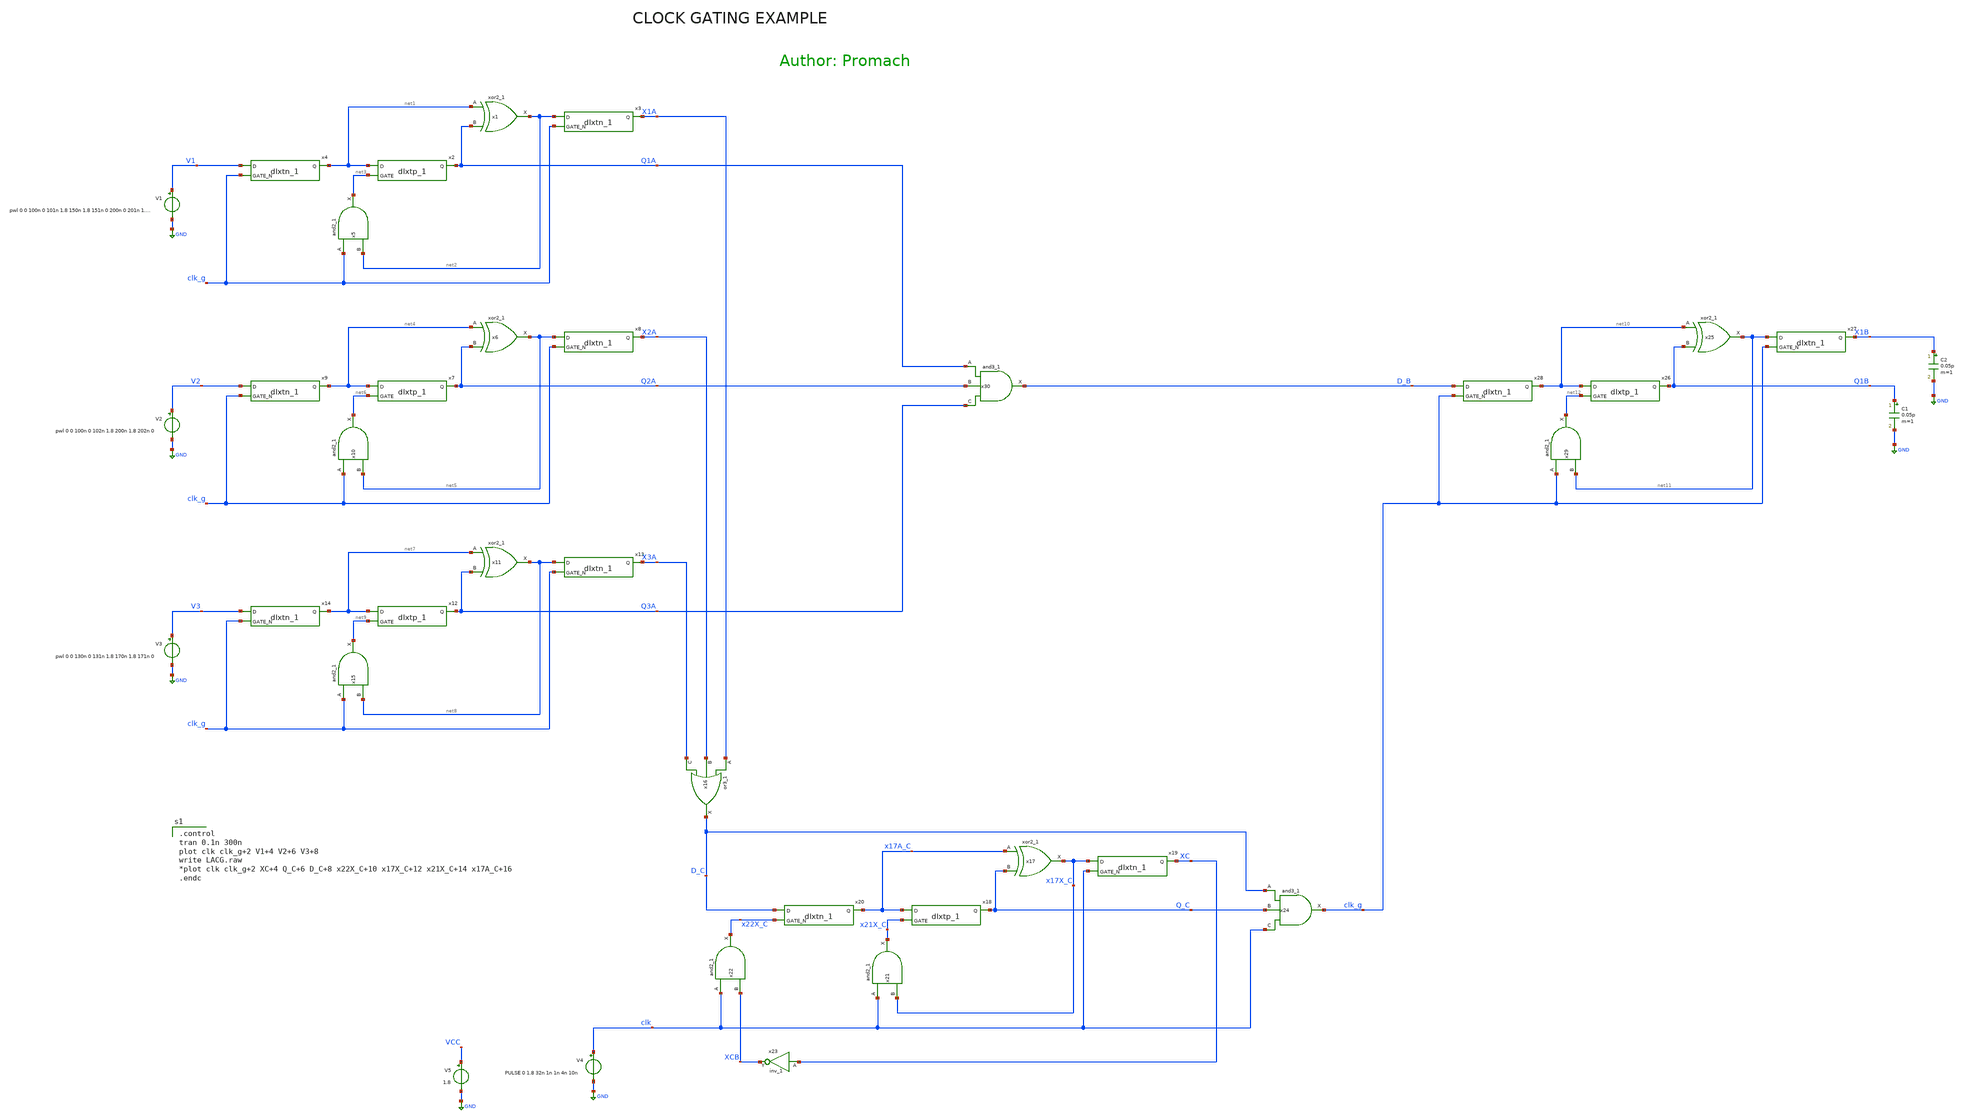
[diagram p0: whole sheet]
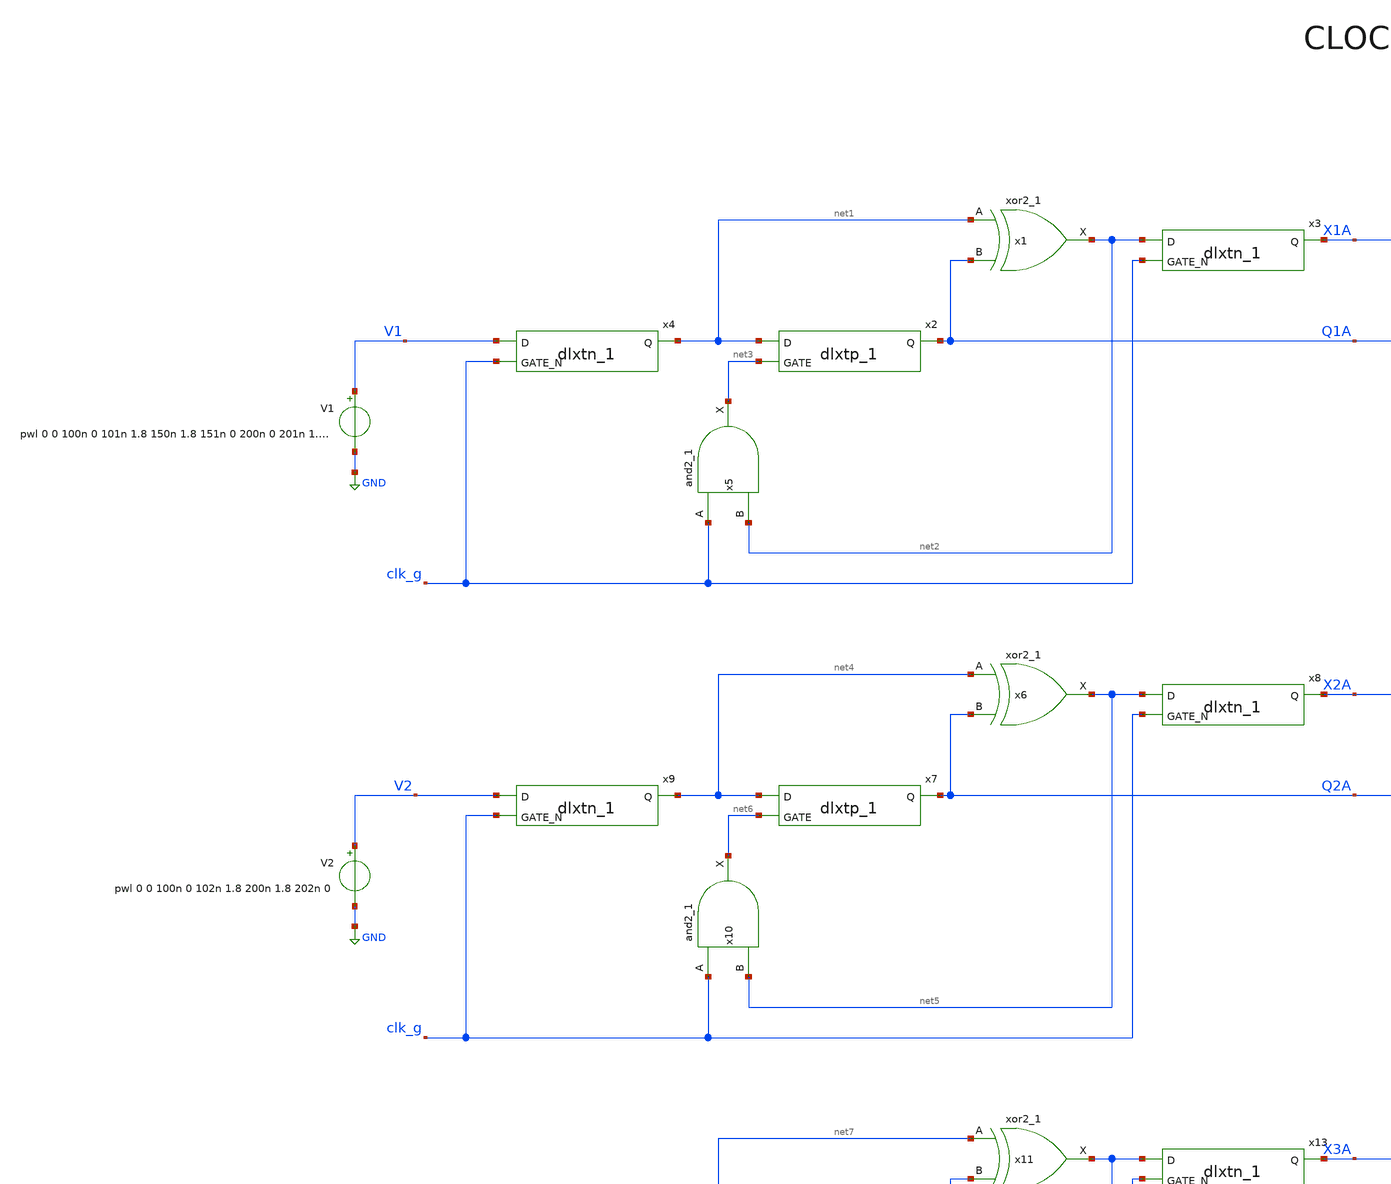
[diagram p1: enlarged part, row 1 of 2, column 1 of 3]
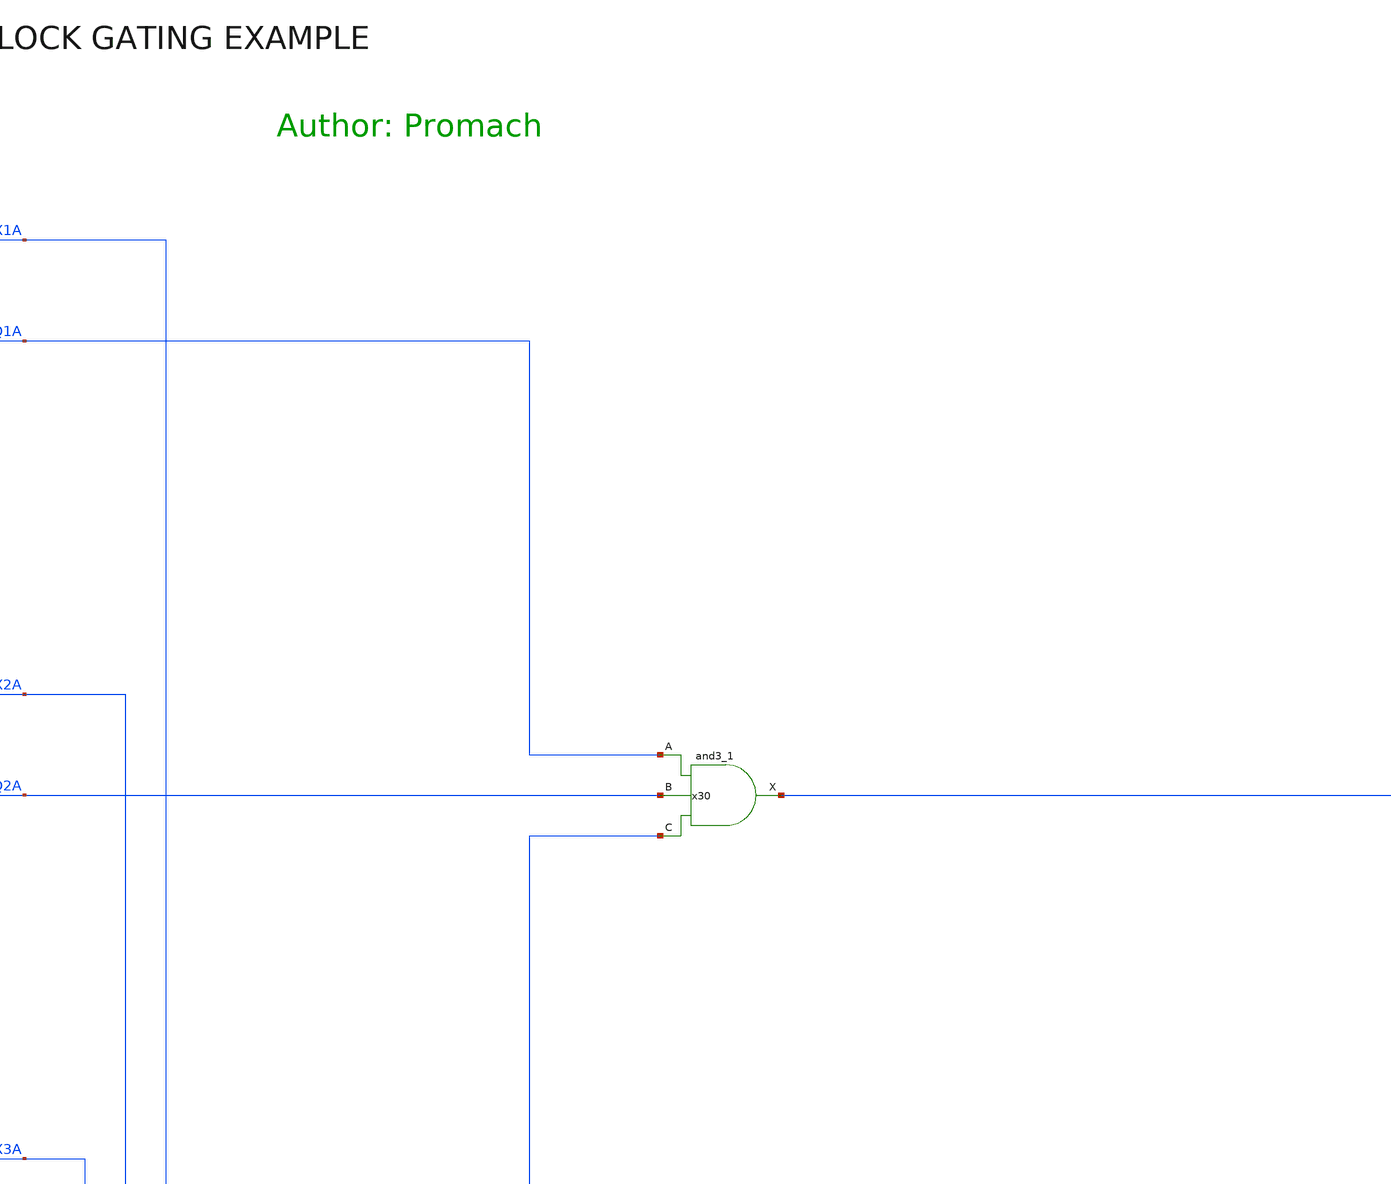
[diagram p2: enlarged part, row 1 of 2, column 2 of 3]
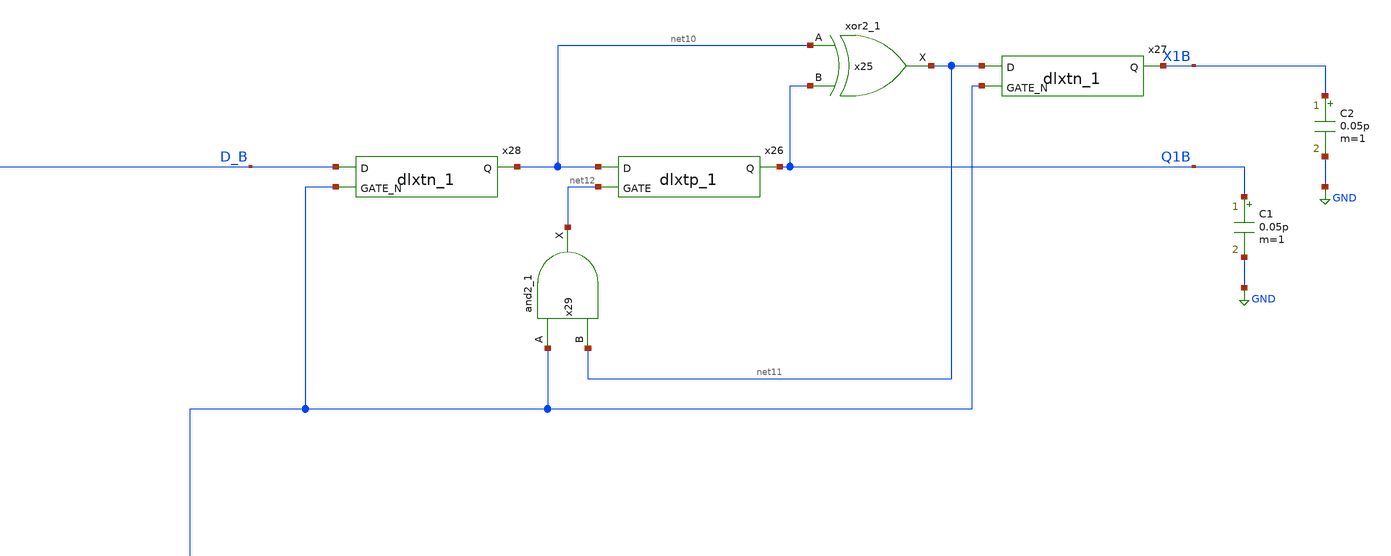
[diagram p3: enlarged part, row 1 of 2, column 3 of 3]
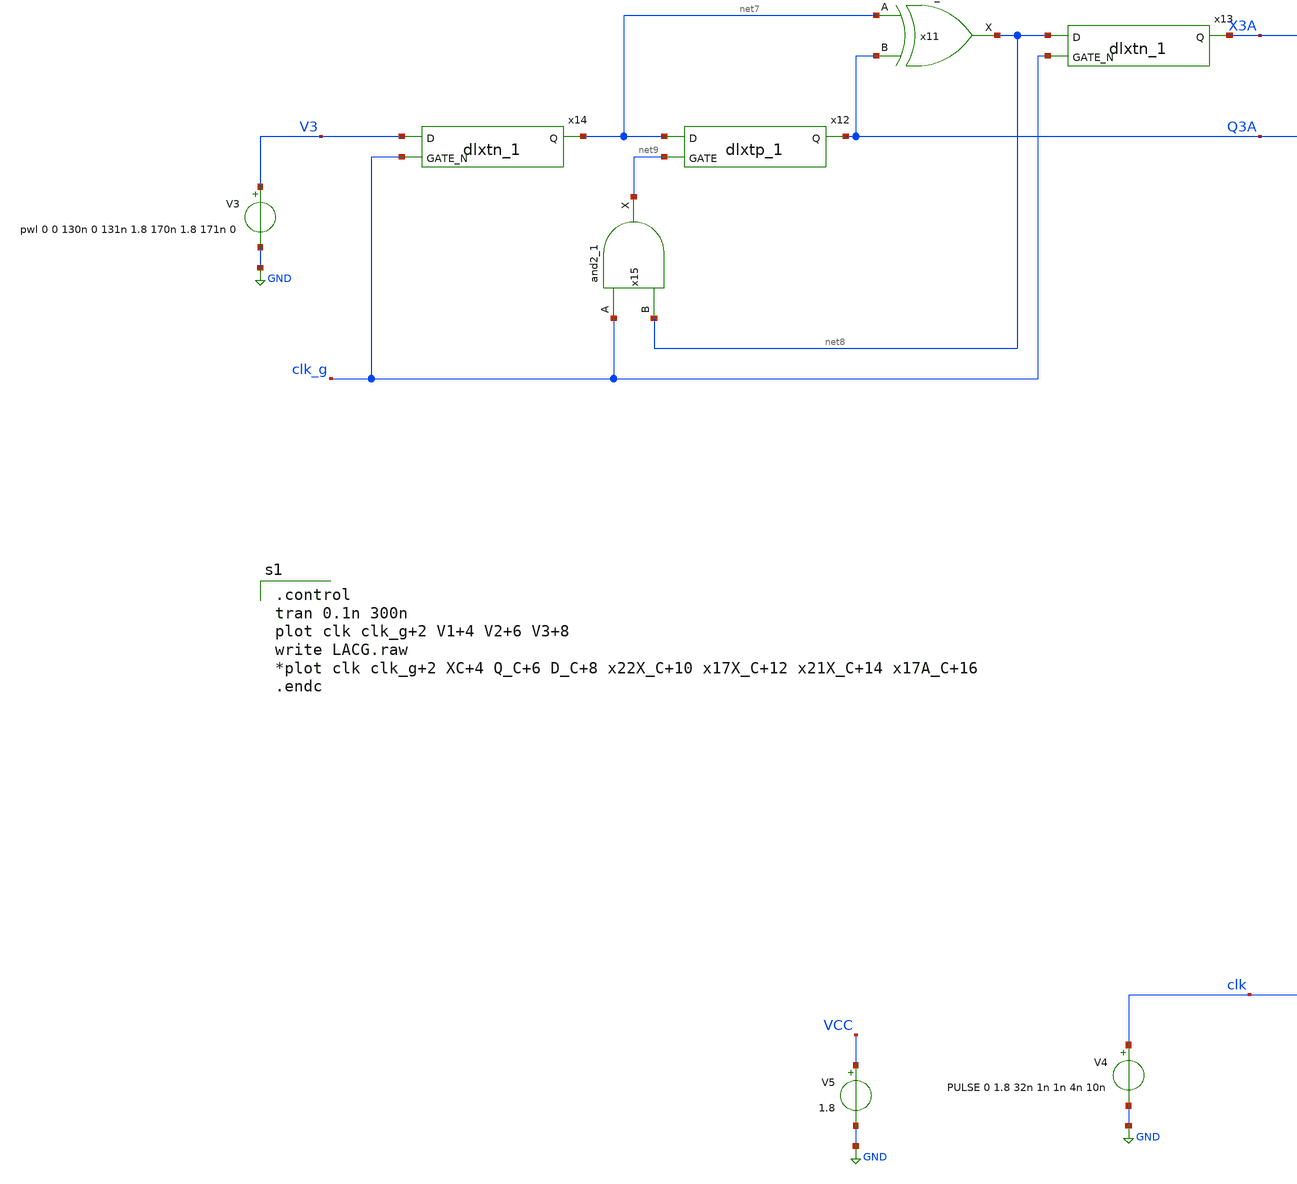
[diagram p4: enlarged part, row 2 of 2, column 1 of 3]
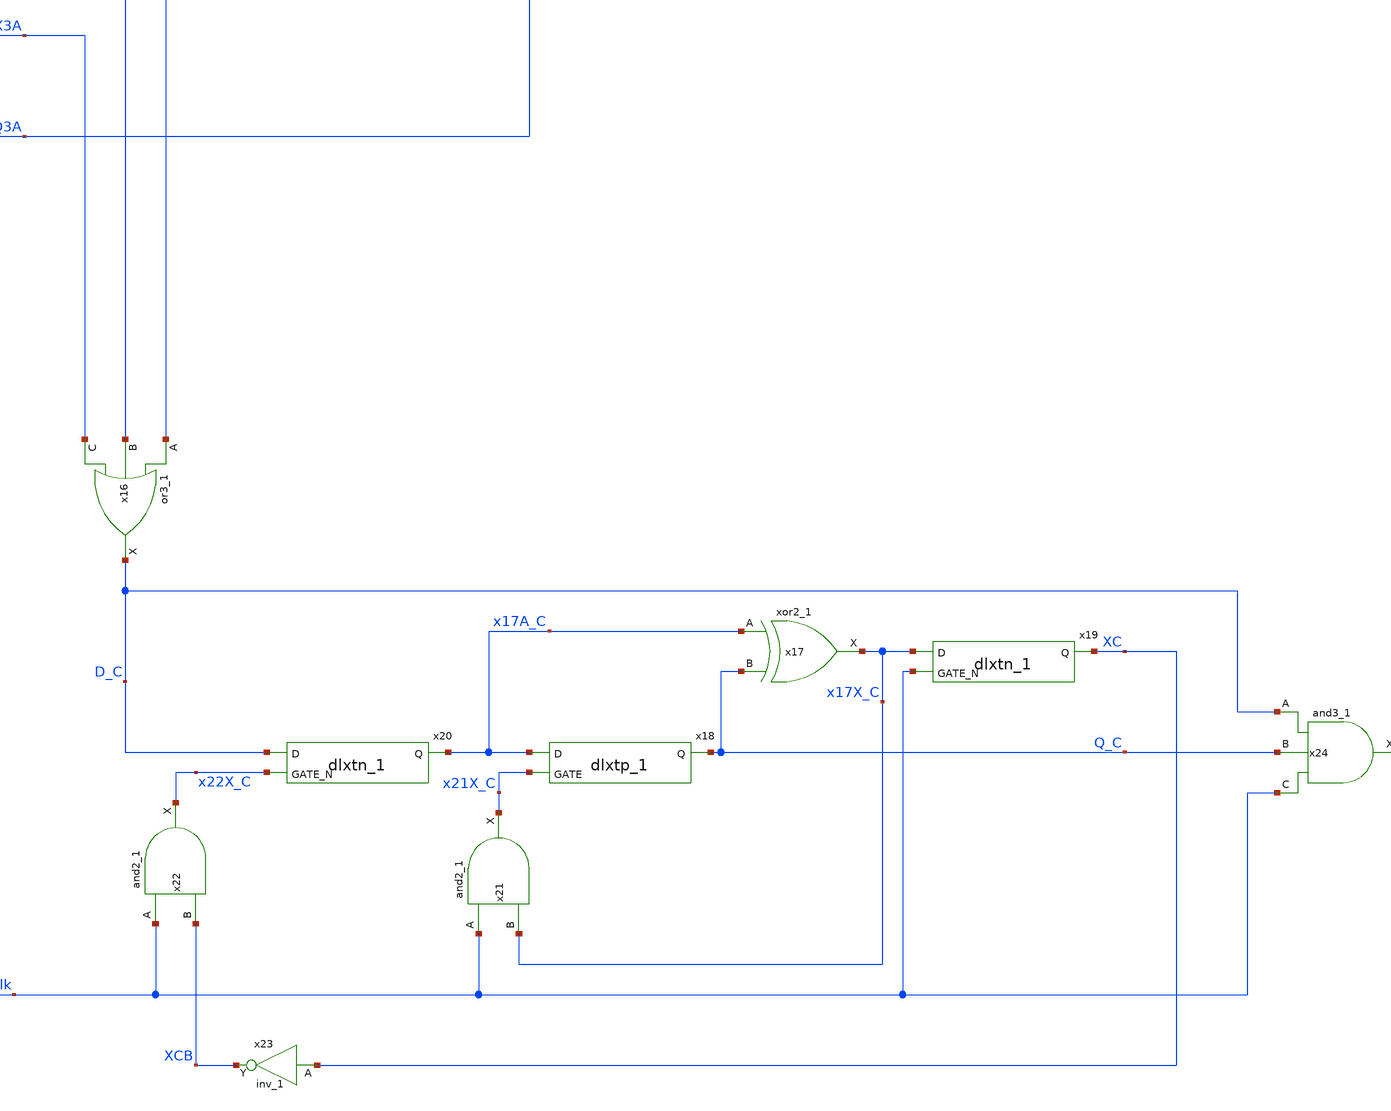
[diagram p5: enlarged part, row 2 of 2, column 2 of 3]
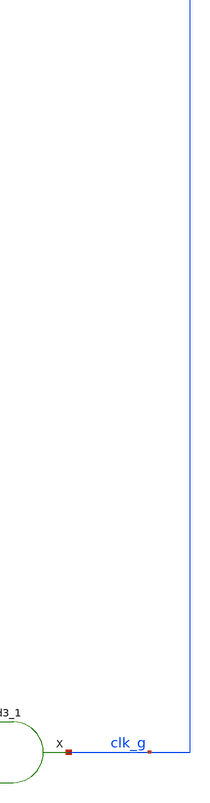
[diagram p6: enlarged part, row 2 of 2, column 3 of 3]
** sch_path: sky130_tests/LACG.sch
**.subckt LACG
x1 net1 Q1A GND GND VCC VCC net2 sky130_fd_sc_hd__xor2_1
x2 net1 net3 GND GND VCC VCC Q1A sky130_fd_sc_hd__dlxtp_1
x3 net2 clk_g GND GND VCC VCC X1A sky130_fd_sc_hd__dlxtn_1
x4 V1 clk_g GND GND VCC VCC net1 sky130_fd_sc_hd__dlxtn_1
x5 clk_g net2 GND GND VCC VCC net3 sky130_fd_sc_hd__and2_1
V1 V1 GND pwl 0 0 100n 0 101n 1.8 150n 1.8 151n 0 200n 0 201n 1.8 231n 1.8
x6 net4 Q2A GND GND VCC VCC net5 sky130_fd_sc_hd__xor2_1
x7 net4 net6 GND GND VCC VCC Q2A sky130_fd_sc_hd__dlxtp_1
x8 net5 clk_g GND GND VCC VCC X2A sky130_fd_sc_hd__dlxtn_1
x9 V2 clk_g GND GND VCC VCC net4 sky130_fd_sc_hd__dlxtn_1
x10 clk_g net5 GND GND VCC VCC net6 sky130_fd_sc_hd__and2_1
x11 net7 Q3A GND GND VCC VCC net8 sky130_fd_sc_hd__xor2_1
x12 net7 net9 GND GND VCC VCC Q3A sky130_fd_sc_hd__dlxtp_1
x13 net8 clk_g GND GND VCC VCC X3A sky130_fd_sc_hd__dlxtn_1
x14 V3 clk_g GND GND VCC VCC net7 sky130_fd_sc_hd__dlxtn_1
x15 clk_g net8 GND GND VCC VCC net9 sky130_fd_sc_hd__and2_1
V2 V2 GND pwl 0 0 100n 0 102n 1.8 200n 1.8 202n 0
V3 V3 GND pwl 0 0 130n 0 131n 1.8 170n 1.8 171n 0
x17 x17A_C Q_C GND GND VCC VCC x17X_C sky130_fd_sc_hd__xor2_1
x18 x17A_C x21X_C GND GND VCC VCC Q_C sky130_fd_sc_hd__dlxtp_1
x19 x17X_C clk GND GND VCC VCC XC sky130_fd_sc_hd__dlxtn_1
x20 D_C x22X_C GND GND VCC VCC x17A_C sky130_fd_sc_hd__dlxtn_1
x21 clk x17X_C GND GND VCC VCC x21X_C sky130_fd_sc_hd__and2_1
x22 clk XCB GND GND VCC VCC x22X_C sky130_fd_sc_hd__and2_1
x23 XC GND GND VCC VCC XCB sky130_fd_sc_hd__inv_1
x24 D_C Q_C clk GND GND VCC VCC clk_g sky130_fd_sc_hd__and3_1
x25 net10 Q1B GND GND VCC VCC net11 sky130_fd_sc_hd__xor2_1
x26 net10 net12 GND GND VCC VCC Q1B sky130_fd_sc_hd__dlxtp_1
x27 net11 clk_g GND GND VCC VCC X1B sky130_fd_sc_hd__dlxtn_1
x28 D_B clk_g GND GND VCC VCC net10 sky130_fd_sc_hd__dlxtn_1
x29 clk_g net11 GND GND VCC VCC net12 sky130_fd_sc_hd__and2_1
C1 Q1B GND 0.05p m=1
C2 X1B GND 0.05p m=1
V4 clk GND PULSE 0 1.8 32n 1n 1n 4n 10n
V5 VCC GND 1.8
x16 X1A X2A X3A GND GND VCC VCC D_C sky130_fd_sc_hd__or3_1
x30 Q1A Q2A Q3A GND GND VCC VCC D_B sky130_fd_sc_hd__and3_1
**** begin user architecture code

.control
tran 0.1n 300n
plot clk clk_g+2 V1+4 V2+6 V3+8
write LACG.raw
*plot clk clk_g+2 XC+4 Q_C+6 D_C+8 x22X_C+10 x17X_C+12 x21X_C+14 x17A_C+16
.endc


 .lib $::SKYWATER_MODELS/sky130.lib.spice tt

.include $::SKYWATER_STDCELLS/sky130_fd_sc_hd.spice

.param mc_mm_switch=0
.param mc_pr_switch=0


**** end user architecture code
**.ends
.GLOBAL GND
.end
